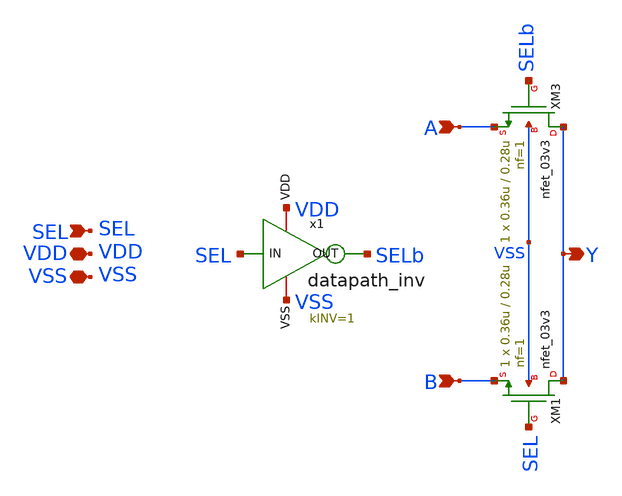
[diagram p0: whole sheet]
** sch_path: CAD7/2x1_mux_pass.sch
**.subckt 2x1_mux_pass A B SEL Y VDD VSS
*.ipin A
*.ipin B
*.ipin SEL
*.opin Y
*.iopin VDD
*.iopin VSS
XM1 Y SEL B VSS nfet_03v3 L=0.28u W=0.36u nf=1 ad='int((nf+1)/2) * W/nf * 0.18u' as='int((nf+2)/2) * W/nf * 0.18u'
+ pd='2*int((nf+1)/2) * (W/nf + 0.18u)' ps='2*int((nf+2)/2) * (W/nf + 0.18u)' nrd='0.18u / W' nrs='0.18u / W'
+ sa=0 sb=0 sd=0 m=1
XM3 Y SELb A VSS nfet_03v3 L=0.28u W=0.36u nf=1 ad='int((nf+1)/2) * W/nf * 0.18u' as='int((nf+2)/2) * W/nf * 0.18u'
+ pd='2*int((nf+1)/2) * (W/nf + 0.18u)' ps='2*int((nf+2)/2) * (W/nf + 0.18u)' nrd='0.18u / W' nrs='0.18u / W'
+ sa=0 sb=0 sd=0 m=1
x1 VDD SEL SELb VSS datapath_inv kINV=1
**.ends
.end
